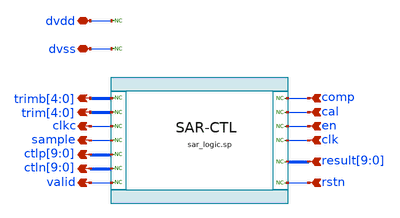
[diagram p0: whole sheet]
** sch_path: xschem/sar_10b/control/sarlogic.sch
**.subckt sarlogic clkc
*+ ctlp[9],ctlp[8],ctlp[7],ctlp[6],ctlp[5],ctlp[4],ctlp[3],ctlp[2],ctlp[1],ctlp[0] ctln[9],ctln[8],ctln[7],ctln[6],ctln[5],ctln[4],ctln[3],ctln[2],ctln[1],ctln[0] sample
*+ trim[4],trim[3],trim[2],trim[1],trim[0] trimb[4],trimb[3],trimb[2],trimb[1],trimb[0] comp cal en clk
*+ result[9],result[8],result[7],result[6],result[5],result[4],result[3],result[2],result[1],result[0] rstn dvdd dvss valid
*.opin clkc
*.opin ctlp[9],ctlp[8],ctlp[7],ctlp[6],ctlp[5],ctlp[4],ctlp[3],ctlp[2],ctlp[1],ctlp[0]
*.opin ctln[9],ctln[8],ctln[7],ctln[6],ctln[5],ctln[4],ctln[3],ctln[2],ctln[1],ctln[0]
*.opin sample
*.opin trim[4],trim[3],trim[2],trim[1],trim[0]
*.opin trimb[4],trimb[3],trimb[2],trimb[1],trimb[0]
*.ipin comp
*.ipin cal
*.ipin en
*.ipin clk
*.ipin
*+ result[9],result[8],result[7],result[6],result[5],result[4],result[3],result[2],result[1],result[0]
*.ipin rstn
*.iopin dvdd
*.iopin dvss
*.opin valid
* noconn comp
* noconn ctlp[9:0]
* noconn ctln[9:0]
* noconn sample
* noconn trimb[4:0]
* noconn trim[4:0]
* noconn result[9:0]
* noconn clkc
* noconn clk
* noconn en
* noconn cal
* noconn rstn
* noconn dvdd
* noconn dvss
* noconn valid
**** begin user architecture code
.include $::DESIGN_PATH/sar_10b/control/cmos_cells_digital.sp
.include $::DESIGN_PATH/sar_10b/control/sarlogic.sp

* Keep the sar_logic underscore name. Otherwise xschem gets confused.
Xuut dclk drstn den dcomp dcal dvalid dres0 dres1 dres2 dres3 dres4 dres5 dres6 dres7 dres8 dres9
+ dsamp dctlp0 dctlp1 dctlp2 dctlp3 dctlp4 dctlp5 dctlp6 dctlp7 dctlp8 dctlp9 dctln0 dctln1 dctln2 dctln3
+ dctln4 dctln5 dctln6 dctln7 dctln8 dctln9 dtrim0 dtrim1 dtrim2 dtrim3 dtrim4 dtrimb0 dtrimb1 dtrimb2
+ dtrimb3 dtrimb4 dclkc sar_logic

.model adc_buff adc_bridge(in_low = 0.2 in_high=0.8)
.model dac_buff dac_bridge(out_high = 1.2)

Aad [clk rstn en comp cal] [dclk drstn den dcomp dcal] adc_buff
Ada1 [dctlp0 dctlp1 dctlp2 dctlp3 dctlp4 dctlp5 dctlp6 dctlp7 dctlp8 dctlp9] [ctlp_0_ ctlp_1_
+ ctlp_2_ ctlp_3_ ctlp_4_ ctlp_5_ ctlp_6_ ctlp_7_ ctlp_8_ ctlp_9_] dac_buff
Ada2 [dctln0 dctln1 dctln2 dctln3 dctln4 dctln5 dctln6 dctln7 dctln8 dctln9] [ctln_0_ ctln_1_
+ ctln_2_ ctln_3_ ctln_4_ ctln_5_ ctln_6_ ctln_7_ ctln_8_ ctln_9_] dac_buff
Ada3 [dres0 dres1 dres2 dres3 dres4 dres5 dres6 dres7 dres8 dres9 dsamp dclkc] [res0 res1 res2 res3
+ res4 res5 res6 res7 res8 res9 sample clkc] dac_buff
Ada4 [dtrim4 dtrim3 dtrim2 dtrim1 dtrim0 dtrimb4 dtrimb3 dtrimb2 dtrimb1 dtrimb0] [trim_4_ trim_3_
+ trim_2_ trim_1_ trim_0_ trimb_4_ trimb_3_ trimb_2_ trimb_1_ trimb_0_ ] dac_buff
Ada5 [dvalid] [valid] dac_buff

**** end user architecture code
**.ends
.end
